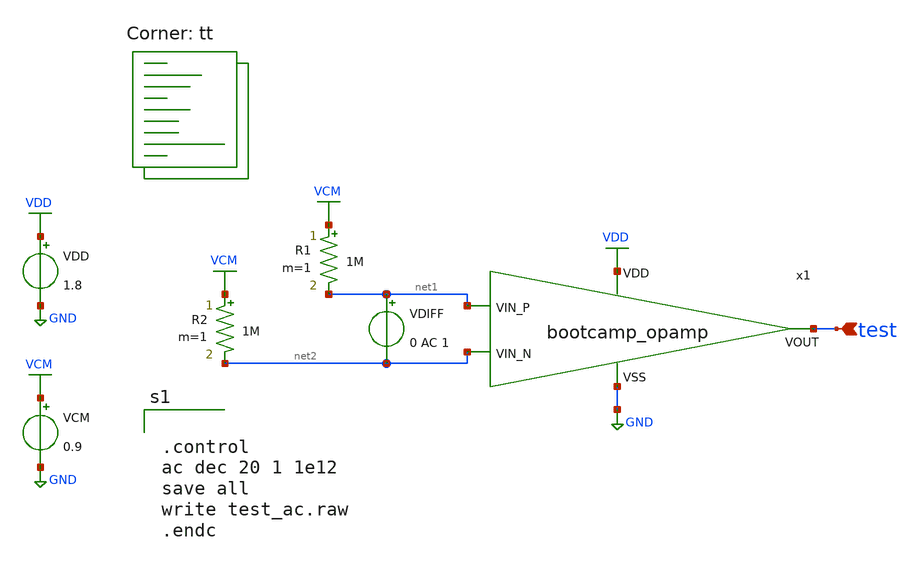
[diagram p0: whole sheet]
** sch_path: analog/schematics/tb_ac_analysis.sch
**.subckt tb_ac_analysis test
*.ipin test
x1 VDD test net2 net1 GND bootcamp_opamp
R1 VCM net1 1M m=1
R2 VCM net2 1M m=1
VDD VDD GND 1.8
VCM VCM GND 0.9
VDIFF net1 net2 0 AC 1
**** begin user architecture code


.control
ac dec 20 1 1e12
save all
write test_ac.raw
.endc


.lib $::SKYWATER_MODELS/sky130.lib.spice tt
**** end user architecture code
**.ends

* expanding   symbol:  bootcamp_opamp.sym # of pins=5
** sym_path: analog/schematics/bootcamp_opamp.sym
** sch_path: analog/schematics/bootcamp_opamp.sch
.subckt bootcamp_opamp VDD VOUT VIN_N VIN_P VSS
*.ipin VIN_P
*.ipin VIN_N
*.ipin VDD
*.ipin VSS
*.opin VOUT
XM1 net1 VIN_P net2 VSS sky130_fd_pr__nfet_01v8 L=1 W=10 nf=1 ad='int((nf+1)/2) * W/nf * 0.29' as='int((nf+2)/2) * W/nf * 0.29'
+ pd='2*int((nf+1)/2) * (W/nf + 0.29)' ps='2*int((nf+2)/2) * (W/nf + 0.29)' nrd='0.29 / W' nrs='0.29 / W'
+ sa=0 sb=0 sd=0 mult=1 m=1
XM2 VOUT VIN_N net2 VSS sky130_fd_pr__nfet_01v8 L=1 W=10 nf=1 ad='int((nf+1)/2) * W/nf * 0.29' as='int((nf+2)/2) * W/nf * 0.29'
+ pd='2*int((nf+1)/2) * (W/nf + 0.29)' ps='2*int((nf+2)/2) * (W/nf + 0.29)' nrd='0.29 / W' nrs='0.29 / W'
+ sa=0 sb=0 sd=0 mult=1 m=1
XM3 net1 net1 VDD VDD sky130_fd_pr__pfet_01v8 L=1 W=30 nf=1 ad='int((nf+1)/2) * W/nf * 0.29' as='int((nf+2)/2) * W/nf * 0.29'
+ pd='2*int((nf+1)/2) * (W/nf + 0.29)' ps='2*int((nf+2)/2) * (W/nf + 0.29)' nrd='0.29 / W' nrs='0.29 / W'
+ sa=0 sb=0 sd=0 mult=1 m=1
XM4 VOUT net1 VDD VDD sky130_fd_pr__pfet_01v8 L=1 W=30 nf=1 ad='int((nf+1)/2) * W/nf * 0.29' as='int((nf+2)/2) * W/nf * 0.29'
+ pd='2*int((nf+1)/2) * (W/nf + 0.29)' ps='2*int((nf+2)/2) * (W/nf + 0.29)' nrd='0.29 / W' nrs='0.29 / W'
+ sa=0 sb=0 sd=0 mult=1 m=1
XM5 net2 net3 VSS VSS sky130_fd_pr__nfet_01v8 L=2 W=10 nf=1 ad='int((nf+1)/2) * W/nf * 0.29' as='int((nf+2)/2) * W/nf * 0.29'
+ pd='2*int((nf+1)/2) * (W/nf + 0.29)' ps='2*int((nf+2)/2) * (W/nf + 0.29)' nrd='0.29 / W' nrs='0.29 / W'
+ sa=0 sb=0 sd=0 mult=1 m=1
XM6 VOUT VOUT VDD VDD sky130_fd_pr__pfet_01v8 L=1 W=30 nf=1 ad='int((nf+1)/2) * W/nf * 0.29' as='int((nf+2)/2) * W/nf * 0.29'
+ pd='2*int((nf+1)/2) * (W/nf + 0.29)' ps='2*int((nf+2)/2) * (W/nf + 0.29)' nrd='0.29 / W' nrs='0.29 / W'
+ sa=0 sb=0 sd=0 mult=1 m=1
XM7 VOUT net3 VSS VSS sky130_fd_pr__nfet_01v8 L=2 W=10 nf=1 ad='int((nf+1)/2) * W/nf * 0.29' as='int((nf+2)/2) * W/nf * 0.29'
+ pd='2*int((nf+1)/2) * (W/nf + 0.29)' ps='2*int((nf+2)/2) * (W/nf + 0.29)' nrd='0.29 / W' nrs='0.29 / W'
+ sa=0 sb=0 sd=0 mult=1 m=1
XM8 net3 net3 VSS VSS sky130_fd_pr__nfet_01v8 L=1 W=20 nf=1 ad='int((nf+1)/2) * W/nf * 0.29' as='int((nf+2)/2) * W/nf * 0.29'
+ pd='2*int((nf+1)/2) * (W/nf + 0.29)' ps='2*int((nf+2)/2) * (W/nf + 0.29)' nrd='0.29 / W' nrs='0.29 / W'
+ sa=0 sb=0 sd=0 mult=1 m=1
I0 VDD net3 200u
**** begin user architecture code
.lib $::SKYWATER_MODELS/sky130.lib.spice tt
**** end user architecture code
.ends

.GLOBAL GND
.GLOBAL VDD
.GLOBAL VCM
.end
